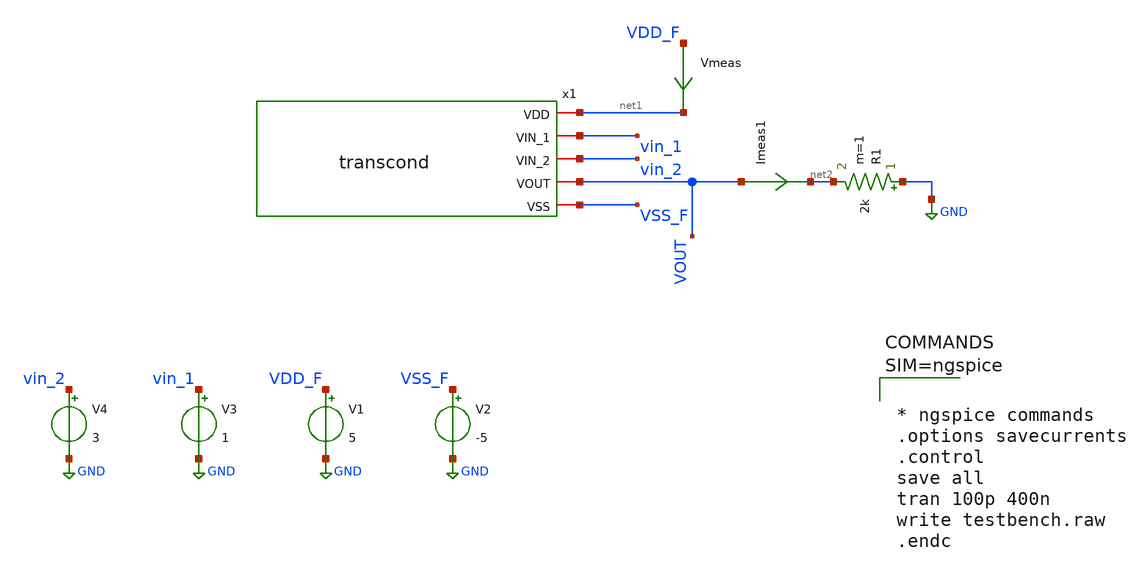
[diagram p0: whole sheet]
** sch_path: xschem/testbench.sch
**.subckt testbench
V1 VDD_F GND 5
V2 VSS_F GND -5
V3 vin_1 GND 1
V4 vin_2 GND 3
Vmeas VDD_F net1 0
.save i(vmeas)
R1 GND net2 2k m=1
Imeas1 VOUT net2 0
.save i(imeas1)
x1 net1 vin_1 vin_2 VOUT VSS_F transcond
**** begin user architecture code

** opencircuitdesign pdks install
.lib $::SKYWATER_MODELS/sky130.lib.spice tt





* ngspice commands
.options savecurrents
.control
save all
tran 100p 400n
write testbench.raw
.endc



**** end user architecture code
**.ends

* expanding   symbol:  transcond.sym # of pins=5
** sym_path: xschem/transcond.sym
** sch_path: xschem/transcond.sch
.subckt transcond VDD VIN_1 VIN_2 VOUT VSS
*.iopin VIN_1
*.iopin VIN_2
*.iopin VOUT
*.iopin VSS
*.iopin VDD
XM3 net1 VIN_2 net2 net2 sky130_fd_pr__nfet_01v8 L=0.3 W=80 nf=30 ad='int((nf+1)/2) * W/nf * 0.29' as='int((nf+2)/2) * W/nf * 0.29'
+ pd='2*int((nf+1)/2) * (W/nf + 0.29)' ps='2*int((nf+2)/2) * (W/nf + 0.29)' nrd='0.29 / W' nrs='0.29 / W'
+ sa=0 sb=0 sd=0 mult=1 m=1
XM7 net3 net3 VSS VSS sky130_fd_pr__nfet_01v8 L=12 W=80 nf=30 ad='int((nf+1)/2) * W/nf * 0.29' as='int((nf+2)/2) * W/nf * 0.29'
+ pd='2*int((nf+1)/2) * (W/nf + 0.29)' ps='2*int((nf+2)/2) * (W/nf + 0.29)' nrd='0.29 / W' nrs='0.29 / W'
+ sa=0 sb=0 sd=0 mult=1 m=1
XM8 net2 net3 VSS VSS sky130_fd_pr__nfet_01v8 L=12 W=80 nf=30 ad='int((nf+1)/2) * W/nf * 0.29' as='int((nf+2)/2) * W/nf * 0.29'
+ pd='2*int((nf+1)/2) * (W/nf + 0.29)' ps='2*int((nf+2)/2) * (W/nf + 0.29)' nrd='0.29 / W' nrs='0.29 / W'
+ sa=0 sb=0 sd=0 mult=1 m=1
XM5 net1 net1 VDD VDD sky130_fd_pr__pfet_01v8 L=12 W=80 nf=30 ad='int((nf+1)/2) * W/nf * 0.29' as='int((nf+2)/2) * W/nf * 0.29'
+ pd='2*int((nf+1)/2) * (W/nf + 0.29)' ps='2*int((nf+2)/2) * (W/nf + 0.29)' nrd='0.29 / W' nrs='0.29 / W'
+ sa=0 sb=0 sd=0 mult=1 m=1
XM6 VOUT net1 VDD VDD sky130_fd_pr__pfet_01v8 L=12 W=80 nf=30 ad='int((nf+1)/2) * W/nf * 0.29' as='int((nf+2)/2) * W/nf * 0.29'
+ pd='2*int((nf+1)/2) * (W/nf + 0.29)' ps='2*int((nf+2)/2) * (W/nf + 0.29)' nrd='0.29 / W' nrs='0.29 / W'
+ sa=0 sb=0 sd=0 mult=1 m=1
R5 VDD net3 600 m=1
XM2 net4 net4 VDD VDD sky130_fd_pr__pfet_01v8 L=12 W=80 nf=30 ad='int((nf+1)/2) * W/nf * 0.29' as='int((nf+2)/2) * W/nf * 0.29'
+ pd='2*int((nf+1)/2) * (W/nf + 0.29)' ps='2*int((nf+2)/2) * (W/nf + 0.29)' nrd='0.29 / W' nrs='0.29 / W'
+ sa=0 sb=0 sd=0 mult=1 m=1
XM4 net5 net4 VDD VDD sky130_fd_pr__pfet_01v8 L=12 W=80 nf=30 ad='int((nf+1)/2) * W/nf * 0.29' as='int((nf+2)/2) * W/nf * 0.29'
+ pd='2*int((nf+1)/2) * (W/nf + 0.29)' ps='2*int((nf+2)/2) * (W/nf + 0.29)' nrd='0.29 / W' nrs='0.29 / W'
+ sa=0 sb=0 sd=0 mult=1 m=1
XM9 net5 net5 VSS VSS sky130_fd_pr__nfet_01v8 L=12 W=180 nf=30 ad='int((nf+1)/2) * W/nf * 0.29' as='int((nf+2)/2) * W/nf * 0.29'
+ pd='2*int((nf+1)/2) * (W/nf + 0.29)' ps='2*int((nf+2)/2) * (W/nf + 0.29)' nrd='0.29 / W' nrs='0.29 / W'
+ sa=0 sb=0 sd=0 mult=1 m=1
XM10 VOUT net5 VSS VSS sky130_fd_pr__nfet_01v8 L=12 W=180 nf=30 ad='int((nf+1)/2) * W/nf * 0.29' as='int((nf+2)/2) * W/nf * 0.29'
+ pd='2*int((nf+1)/2) * (W/nf + 0.29)' ps='2*int((nf+2)/2) * (W/nf + 0.29)' nrd='0.29 / W' nrs='0.29 / W'
+ sa=0 sb=0 sd=0 mult=1 m=1
XM1 net4 VIN_1 net2 net2 sky130_fd_pr__nfet_01v8 L=0.3 W=80 nf=30 ad='int((nf+1)/2) * W/nf * 0.29' as='int((nf+2)/2) * W/nf * 0.29'
+ pd='2*int((nf+1)/2) * (W/nf + 0.29)' ps='2*int((nf+2)/2) * (W/nf + 0.29)' nrd='0.29 / W' nrs='0.29 / W'
+ sa=0 sb=0 sd=0 mult=1 m=1
.ends

.GLOBAL GND
.end
